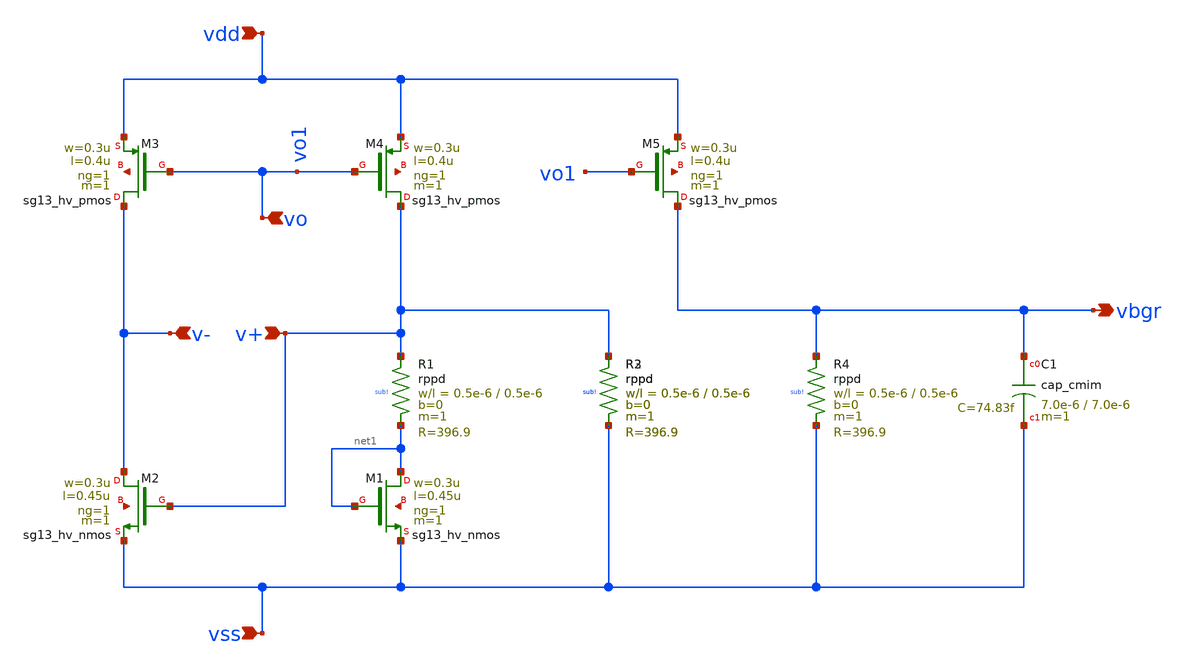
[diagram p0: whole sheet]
** sch_path: schematic/bandgap_ref.sch
**.subckt bandgap_ref vdd vss v+ v- vo vbgr
*.ipin vdd
*.ipin vss
*.ipin v+
*.ipin v-
*.ipin vo
*.opin vbgr
XM1 net1 net1 vss net2 sg13_hv_nmos w=0.3u l=0.45u ng=1 m=1 mm_ok=1
XM2 v- v+ vss net3 sg13_hv_nmos w=0.3u l=0.45u ng=1 m=1 mm_ok=1
XM3 v- vo vdd net4 sg13_hv_pmos w=0.3u l=0.4u ng=1 m=1 mm_ok=1
XM4 v+ vo vdd net5 sg13_hv_pmos w=0.3u l=0.4u ng=1 m=1 mm_ok=1
XR1 v+ net1 sub! rppd w=0.5e-6 l=0.5e-6 m=1 b=0 mm_ok=1
XR2 v+ vss sub! rppd w=0.5e-6 l=0.5e-6 m=1 b=0 mm_ok=1
XM5 vbgr vo1 vdd net6 sg13_hv_pmos w=0.3u l=0.4u ng=1 m=1 mm_ok=1
XR3 v+ vss sub! rppd w=0.5e-6 l=0.5e-6 m=1 b=0 mm_ok=1
XR4 vbgr vss sub! rppd w=0.5e-6 l=0.5e-6 m=1 b=0 mm_ok=1
XC1 vbgr vss cap_cmim w=7.0e-6 l=7.0e-6 m=1 mm_ok=1
**.ends
.end
